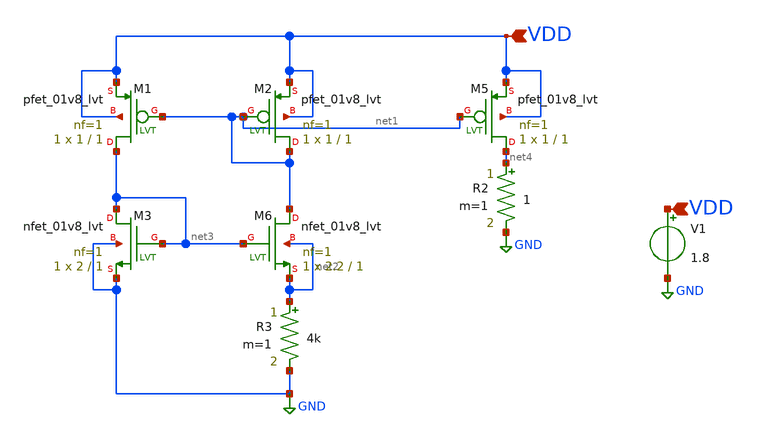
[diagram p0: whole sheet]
** sch_path: xschem/currentsource.sch
**.subckt currentsource VDD VDD
*.ipin VDD
*.ipin VDD
XM2 net1 net1 VDD VDD sky130_fd_pr__pfet_01v8_lvt L=1 W=1 nf=1 ad='int((1 + 1)/2) * 1 / 1 * 0.29' as='int((1 + 2)/2) * 1 / 1 * 0.29'
+ pd='2*int((1 + 1)/2) * (1 / 1 + 0.29)' ps='2*int((1 + 2)/2) * (1 / 1 + 0.29)' nrd='0.29 / 1 ' nrs='0.29 / 1 '
+ sa=0 sb=0 sd=0 mult=1 m=1
XM1 net3 net1 VDD VDD sky130_fd_pr__pfet_01v8_lvt L=1 W=1 nf=1 ad='int((1 + 1)/2) * 1 / 1 * 0.29' as='int((1 + 2)/2) * 1 / 1 * 0.29'
+ pd='2*int((1 + 1)/2) * (1 / 1 + 0.29)' ps='2*int((1 + 2)/2) * (1 / 1 + 0.29)' nrd='0.29 / 1 ' nrs='0.29 / 1 '
+ sa=0 sb=0 sd=0 mult=1 m=1
V1 VDD GND 1.8
XM5 net4 net1 VDD VDD sky130_fd_pr__pfet_01v8_lvt L=1 W=1 nf=1 ad='int((1 + 1)/2) * 1 / 1 * 0.29' as='int((1 + 2)/2) * 1 / 1 * 0.29'
+ pd='2*int((1 + 1)/2) * (1 / 1 + 0.29)' ps='2*int((1 + 2)/2) * (1 / 1 + 0.29)' nrd='0.29 / 1 ' nrs='0.29 / 1 '
+ sa=0 sb=0 sd=0 mult=1 m=1
R2 net4 GND 1 m=1
R3 net2 GND 4k m=1
XM6 net1 net3 net2 net2 sky130_fd_pr__nfet_01v8_lvt L=1 W=2.2 nf=1 ad='int((1 + 1)/2) * 2.2 / 1 * 0.29'
+ as='int((1 + 2)/2) * 2.2 / 1 * 0.29' pd='2*int((1 + 1)/2) * (2.2 / 1 + 0.29)' ps='2*int((1 + 2)/2) * (2.2 / 1 + 0.29)'
+ nrd='0.29 / 2.2 ' nrs='0.29 / 2.2 ' sa=0 sb=0 sd=0 mult=1 m=1
XM3 net3 net3 GND GND sky130_fd_pr__nfet_01v8_lvt L=1 W=2 nf=1 ad='int((1 + 1)/2) * 2 / 1 * 0.29' as='int((1 + 2)/2) * 2 / 1 * 0.29'
+ pd='2*int((1 + 1)/2) * (2 / 1 + 0.29)' ps='2*int((1 + 2)/2) * (2 / 1 + 0.29)' nrd='0.29 / 2 ' nrs='0.29 / 2 '
+ sa=0 sb=0 sd=0 mult=1 m=1
**** begin user architecture code



.lib /usr/local/share/pdk/sky130A/libs.tech/ngspice/sky130.lib.spice tt
.tran 5u 10u
.save all

.control
run
print -i(v1)
set wr_singlescale
set wr_vecnames
*wrdata /foss/designs/2stageCMOSOpAmp/sim_data/GainvsFreq/gain(max).txt db(vout/v(v+))
*wrdata /foss/designs/2stageCMOSOpAmp/sim_data/sample_waves/a1.3m_f1k_gain700.txt vout
*wrdata /foss/designs/2stageCMOSOpAmp/sim_data/SR/SR.txt vout

.endc


**** end user architecture code
**.ends
.GLOBAL GND
.end
